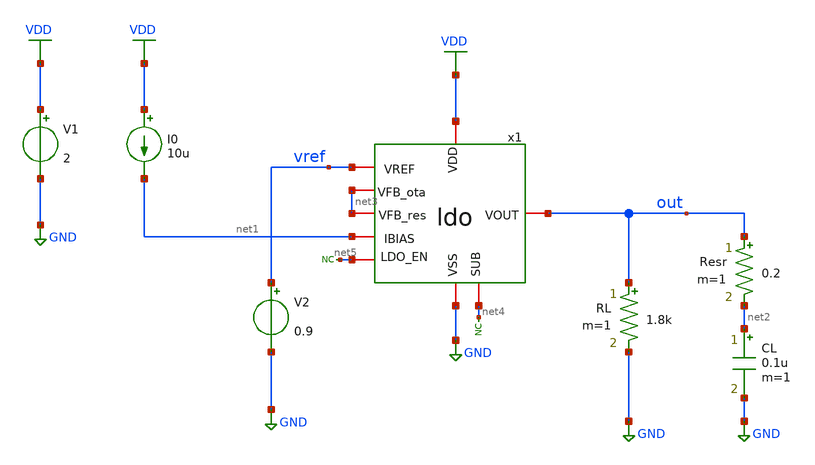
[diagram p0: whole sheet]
** sch_path: designs/libs/tb_ldo/tb_ldo_noise/tb_ldo_noise.sch
**.subckt tb_ldo_noise
* noconn #net5
RL out GND 1.8k m=1
V1 VDD GND 2
V2 vref GND 0.9
I0 VDD net1 10u
CL net2 GND 0.1u m=1
Resr out net2 0.2 m=1
x1 VDD vref out net1 net4 GND net5 net3 net3 ldo
* noconn #net4
**** begin user architecture code



.control
save all

run
set color0 = white

** Set sources
alter @V1[AC] = 1

** Simulation
op
noise v(out) V1 dec 100 1 10G

** Plots
setplot noise1
plot onoise_spectrum
plot inoise_spectrum

** Measurements
let output_noise_at_1MHz = onoise_spectrum[600]
print output_noise_at_1MHz

write tb_ldo_noise.raw
.endc
* ngspice commands




.include $::180MCU_MODELS/design.ngspice
.lib $::180MCU_MODELS/sm141064.ngspice typical
.lib $::180MCU_MODELS/sm141064.ngspice cap_mim
.lib $::180MCU_MODELS/sm141064.ngspice moscap_typical
.lib $::180MCU_MODELS/sm141064.ngspice mimcap_typical
.lib $::180MCU_MODELS/sm141064.ngspice res_typical
* .lib $::180MCU_MODELS/sm141064.ngspice res_statistical
* ngspice commands

**** end user architecture code
**.ends
.GLOBAL GND
.GLOBAL VDD
.end
